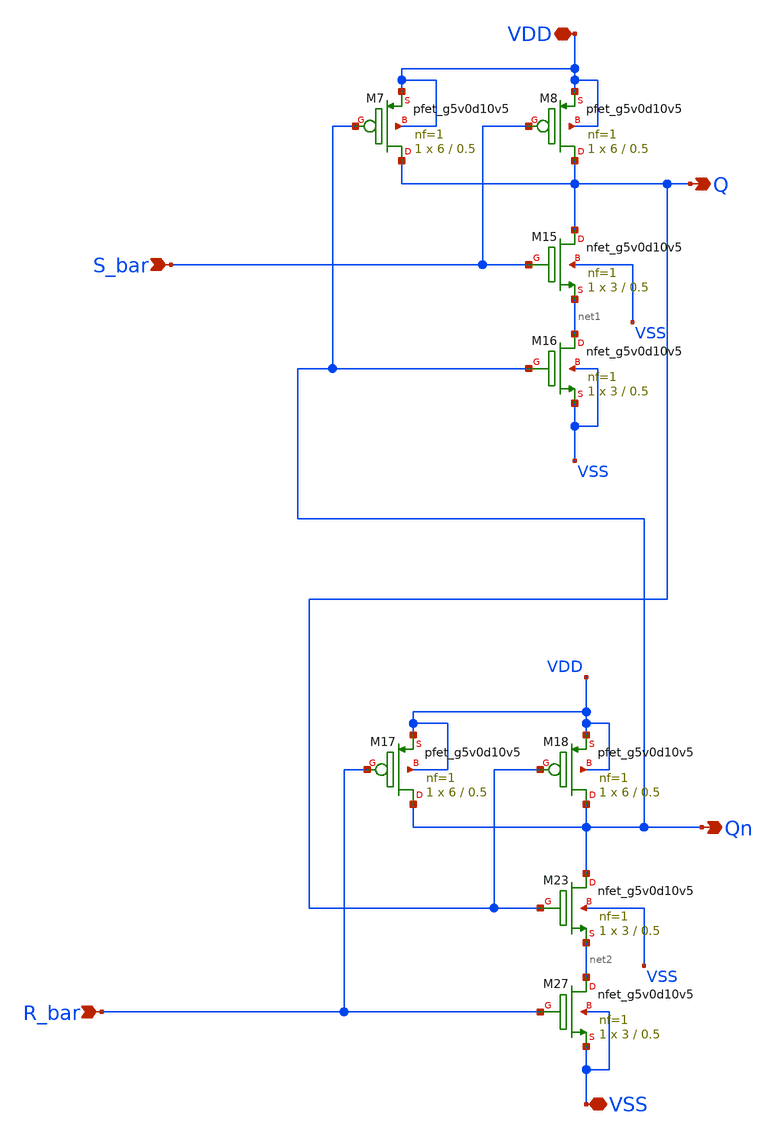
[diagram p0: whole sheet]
** sch_path: xschem/SR.sch
**.subckt SR VDD Qn Q S_bar R_bar VSS
*.iopin VDD
*.opin Qn
*.opin Q
*.ipin S_bar
*.ipin R_bar
*.iopin VSS
XM7 Q Qn VDD VDD sky130_fd_pr__pfet_g5v0d10v5 L=0.5 W=6 nf=1 ad='int((1 + 1)/2) * 6 / 1 * 0.29' as='int((1 + 2)/2) * 6 / 1 * 0.29'
+ pd='2*int((1 + 1)/2) * (6 / 1 + 0.29)' ps='2*int((1 + 2)/2) * (6 / 1 + 0.29)' nrd='0.29 / 6 ' nrs='0.29 / 6 '
+ sa=0 sb=0 sd=0 mult=1 m=1
XM8 Q S_bar VDD VDD sky130_fd_pr__pfet_g5v0d10v5 L=0.5 W=6 nf=1 ad='int((1 + 1)/2) * 6 / 1 * 0.29' as='int((1 + 2)/2) * 6 / 1 * 0.29'
+ pd='2*int((1 + 1)/2) * (6 / 1 + 0.29)' ps='2*int((1 + 2)/2) * (6 / 1 + 0.29)' nrd='0.29 / 6 ' nrs='0.29 / 6 '
+ sa=0 sb=0 sd=0 mult=1 m=1
XM15 Q S_bar net1 VSS sky130_fd_pr__nfet_g5v0d10v5 L=0.5 W=3 nf=1 ad='int((1 + 1)/2) * 3 / 1 * 0.29'
+ as='int((1 + 2)/2) * 3 / 1 * 0.29' pd='2*int((1 + 1)/2) * (3 / 1 + 0.29)' ps='2*int((1 + 2)/2) * (3 / 1 + 0.29)'
+ nrd='0.29 / 3 ' nrs='0.29 / 3 ' sa=0 sb=0 sd=0 mult=1 m=1
XM16 net1 Qn VSS VSS sky130_fd_pr__nfet_g5v0d10v5 L=0.5 W=3 nf=1 ad='int((1 + 1)/2) * 3 / 1 * 0.29' as='int((1 + 2)/2) * 3 / 1 * 0.29'
+ pd='2*int((1 + 1)/2) * (3 / 1 + 0.29)' ps='2*int((1 + 2)/2) * (3 / 1 + 0.29)' nrd='0.29 / 3 ' nrs='0.29 / 3 '
+ sa=0 sb=0 sd=0 mult=1 m=1
XM17 Qn R_bar VDD VDD sky130_fd_pr__pfet_g5v0d10v5 L=0.5 W=6 nf=1 ad='int((1 + 1)/2) * 6 / 1 * 0.29'
+ as='int((1 + 2)/2) * 6 / 1 * 0.29' pd='2*int((1 + 1)/2) * (6 / 1 + 0.29)' ps='2*int((1 + 2)/2) * (6 / 1 + 0.29)'
+ nrd='0.29 / 6 ' nrs='0.29 / 6 ' sa=0 sb=0 sd=0 mult=1 m=1
XM18 Qn Q VDD VDD sky130_fd_pr__pfet_g5v0d10v5 L=0.5 W=6 nf=1 ad='int((1 + 1)/2) * 6 / 1 * 0.29' as='int((1 + 2)/2) * 6 / 1 * 0.29'
+ pd='2*int((1 + 1)/2) * (6 / 1 + 0.29)' ps='2*int((1 + 2)/2) * (6 / 1 + 0.29)' nrd='0.29 / 6 ' nrs='0.29 / 6 '
+ sa=0 sb=0 sd=0 mult=1 m=1
XM23 Qn Q net2 VSS sky130_fd_pr__nfet_g5v0d10v5 L=0.5 W=3 nf=1 ad='int((1 + 1)/2) * 3 / 1 * 0.29' as='int((1 + 2)/2) * 3 / 1 * 0.29'
+ pd='2*int((1 + 1)/2) * (3 / 1 + 0.29)' ps='2*int((1 + 2)/2) * (3 / 1 + 0.29)' nrd='0.29 / 3 ' nrs='0.29 / 3 '
+ sa=0 sb=0 sd=0 mult=1 m=1
XM27 net2 R_bar VSS VSS sky130_fd_pr__nfet_g5v0d10v5 L=0.5 W=3 nf=1 ad='int((1 + 1)/2) * 3 / 1 * 0.29'
+ as='int((1 + 2)/2) * 3 / 1 * 0.29' pd='2*int((1 + 1)/2) * (3 / 1 + 0.29)' ps='2*int((1 + 2)/2) * (3 / 1 + 0.29)'
+ nrd='0.29 / 3 ' nrs='0.29 / 3 ' sa=0 sb=0 sd=0 mult=1 m=1
**.ends
.end
